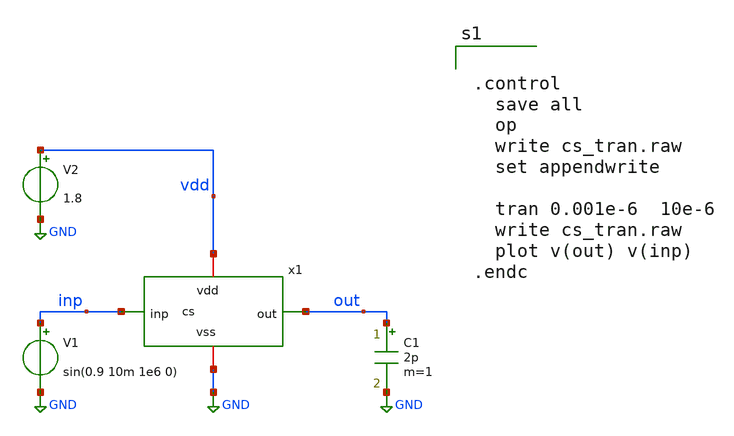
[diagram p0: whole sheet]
** sch_path: xschem/cs_tran.sch
**.subckt cs_tran
x1 out inp vdd GND cs
V1 inp GND sin(0.9 10m 1e6 0)
V2 vdd GND 1.8
C1 out GND 2p m=1
**** begin user architecture code

** opencircuitdesign pdks install
.lib $::SKYWATER_MODELS/sky130.lib.spice tt




.control
  save all
  op
  write cs_tran.raw
  set appendwrite

  tran 0.001e-6  10e-6
  write cs_tran.raw
  plot v(out) v(inp)
.endc


**** end user architecture code
**.ends

* expanding   symbol:  cs.sym # of pins=4
** sym_path: xschem/cs.sym
.include cs_pex.spice
.GLOBAL GND
.end
